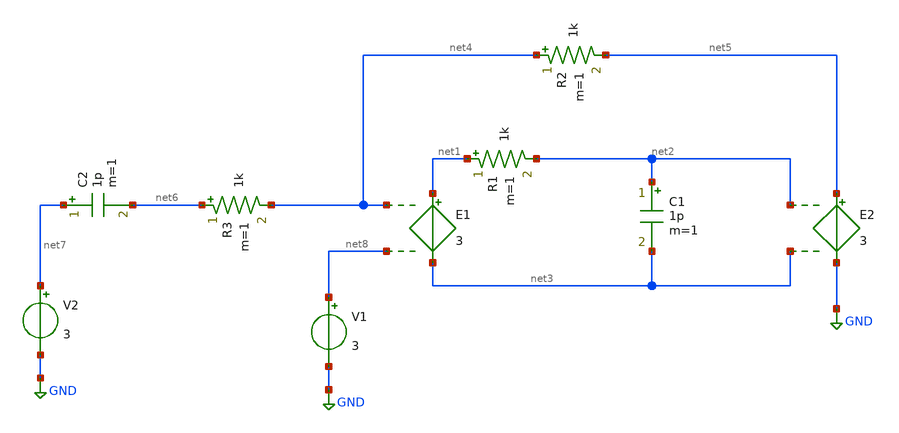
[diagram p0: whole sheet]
** sch_path: xschem/task2.sch
**.subckt task2
E1 net1 net3 net4 net8 3
E2 net5 GND net2 net3 3
R1 net1 net2 1k m=1
C1 net2 net3 1p m=1
R2 net4 net5 1k m=1
V1 net8 GND 3
R3 net6 net4 1k m=1
C2 net7 net6 1p m=1
V2 net7 GND 3
**.ends
.GLOBAL GND
.end
